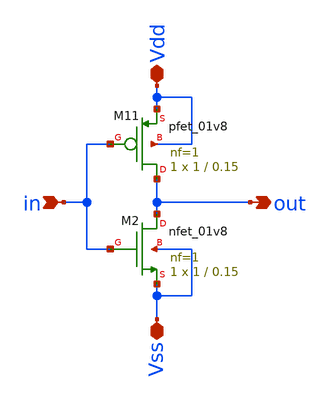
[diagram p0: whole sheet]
** sch_path: inv/inverter.sch
**.subckt inverter in Vdd Vss out
*.ipin in
*.iopin Vdd
*.iopin Vss
*.opin out
XM2 out in Vss Vss sky130_fd_pr__nfet_01v8 L=0.15 W=1 nf=1 ad='int((1 + 1)/2) * 1 / 1 * 0.29' as='int((1 + 2)/2) * 1 / 1 * 0.29'
+ pd='2*int((1 + 1)/2) * (1 / 1 + 0.29)' ps='2*int((1 + 2)/2) * (1 / 1 + 0.29)' nrd='0.29 / 1 ' nrs='0.29 / 1 '
+ sa=0 sb=0 sd=0 mult=1 m=1
XM11 out in Vdd Vdd sky130_fd_pr__pfet_01v8 L=0.15 W=1 nf=1 ad='int((nf+1)/2) * W/nf * 0.29' as='int((nf+2)/2) * W/nf * 0.29'
+ pd='2*int((nf+1)/2) * (W/nf + 0.29)' ps='2*int((nf+2)/2) * (W/nf + 0.29)' nrd='0.29 / W' nrs='0.29 / W'
+ sa=0 sb=0 sd=0 mult=1 m=1
**** begin user architecture code

** opencircuitdesign pdks install
.lib $::SKYWATER_MODELS/sky130.lib.spice tt_mm


**** end user architecture code
**.ends
.end
